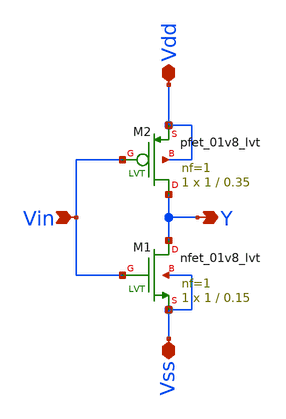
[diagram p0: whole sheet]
** sch_path: inverter_hierarchical/inverter.sch
**.subckt inverter Y Vdd Vin Vss
*.opin Y
*.iopin Vdd
*.ipin Vin
*.iopin Vss
XM1 Y Vin Vss Vss sky130_fd_pr__nfet_01v8_lvt L=0.15 W=1 nf=1 ad='int((nf+1)/2) * W/nf * 0.29' as='int((nf+2)/2) * W/nf * 0.29'
+ pd='2*int((nf+1)/2) * (W/nf + 0.29)' ps='2*int((nf+2)/2) * (W/nf + 0.29)' nrd='0.29 / W' nrs='0.29 / W'
+ sa=0 sb=0 sd=0 mult=1 m=1
XM2 Y Vin Vdd Vdd sky130_fd_pr__pfet_01v8_lvt L=0.35 W=1 nf=1 ad='int((nf+1)/2) * W/nf * 0.29' as='int((nf+2)/2) * W/nf * 0.29'
+ pd='2*int((nf+1)/2) * (W/nf + 0.29)' ps='2*int((nf+2)/2) * (W/nf + 0.29)' nrd='0.29 / W' nrs='0.29 / W'
+ sa=0 sb=0 sd=0 mult=1 m=1
**.ends
.end
